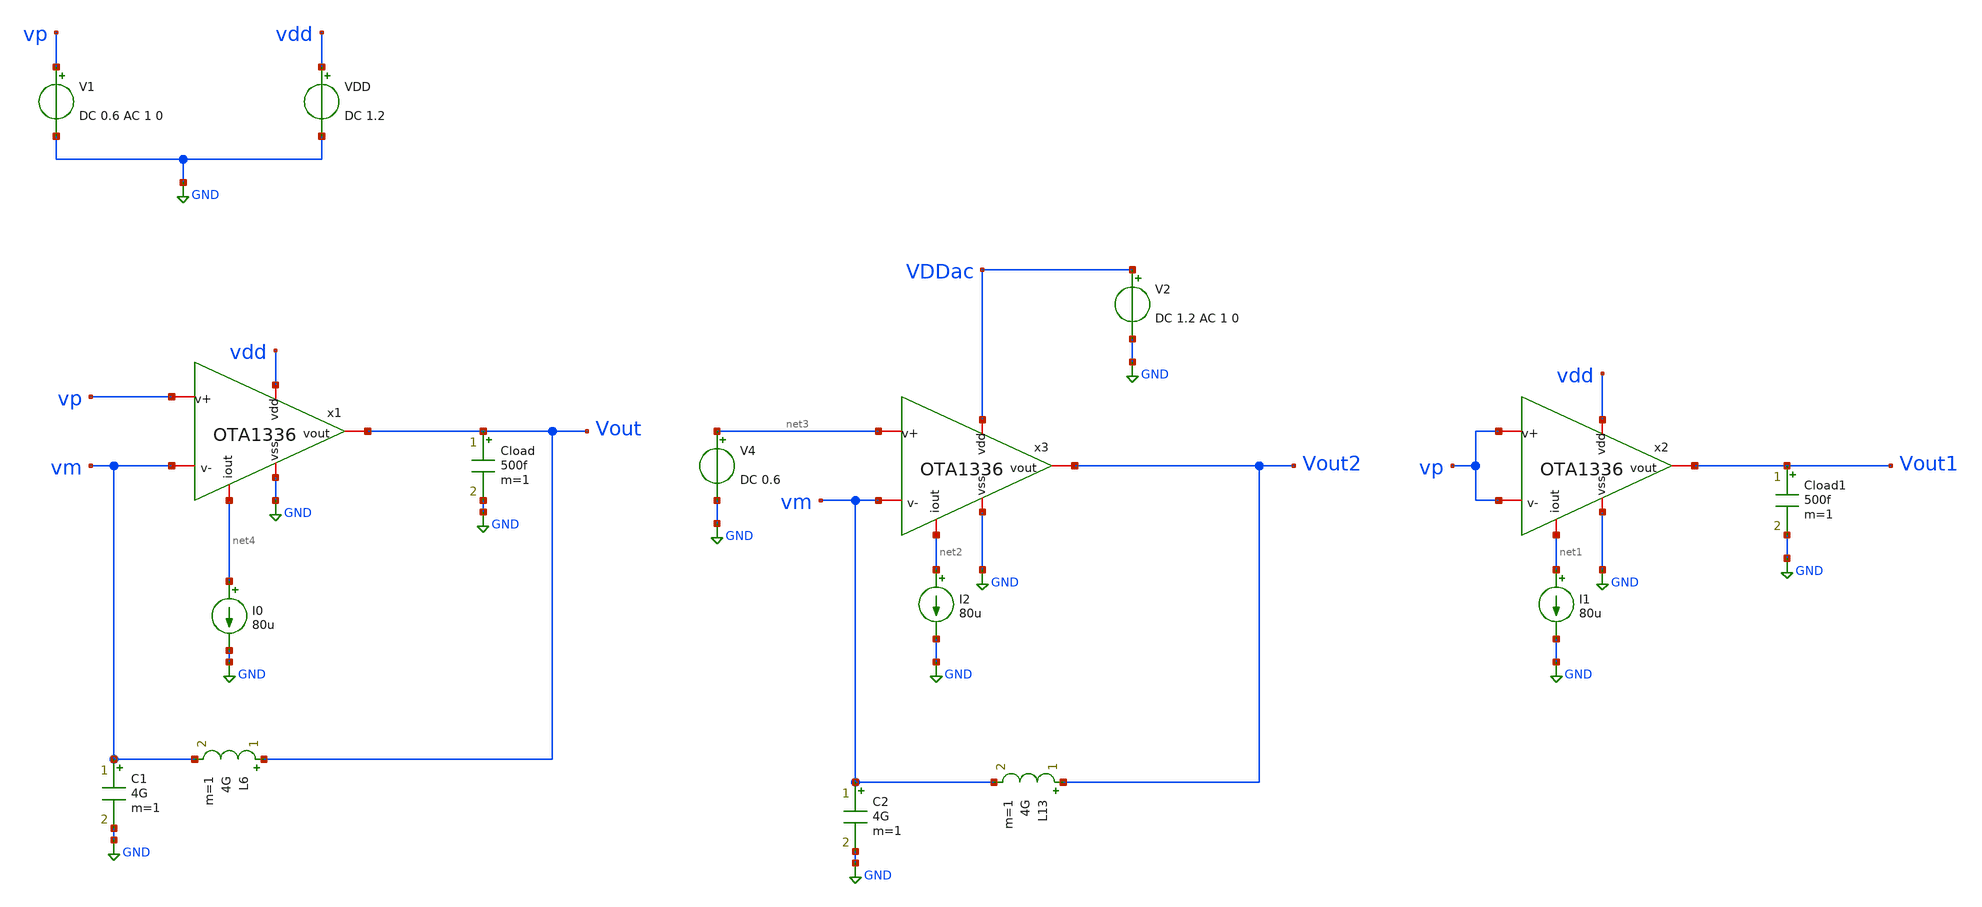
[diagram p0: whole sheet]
** sch_path: OTA1336-main/testbenches/ac/xschem/OTA1336_tb.sch
**.subckt OTA1336_tb
V1 vp GND DC 0.6 AC 1 0
VDD vdd GND DC 1.2
I0 net4 GND 80u
Cload Vout GND 500f m=1
L6 Vout vm 4G m=1
C1 vm GND 4G m=1
I1 net1 GND 80u
Cload1 Vout1 GND 500f m=1
I2 net2 GND 80u
L13 Vout2 vm 4G m=1
C2 vm GND 4G m=1
V2 VDDac GND DC 1.2 AC 1 0
V4 net3 GND DC 0.6
x1 vdd net4 Vout vm vp GND OTA1336
x2 vdd net1 Vout1 vp vp GND OTA1336
x3 VDDac net2 Vout2 vm net3 GND OTA1336
**** begin user architecture code

.lib cornerCAP.lib cap_typ
.lib cornerMOSlv.lib mos_tt
.lib cornerRES.lib res_typ



.control
op
save all
write tb_OTA_op.raw
.endc

.control
op
ac dec 100 1 10e7
save all
let Av = db(v(vout) / v(vp))
let vph = -180*unwrap(phase(V(vout)) - phase(V(vp)))/pi
let PSRR_linear = v(vout2)/v(VDDac)
let CMRR = db((v(vout)/v(vp))/(v(vout1)/v(vp)))
let phase = 180*cph(vout)/pi

let vog = db(V(vout)/V(vp))
let vph = 180 * unwrap(phase(V(vout)) - phase(V(vp)))/pi
let fbw = 0
let pm = 0
let gm = minimum(vog)
meas ac fbw WHEN vog=1 FALL=1
meas ac pm FIND vph WHEN vog=0 FALL=1
meas ac gm FIND vog WHEN vph=-180 FALL=1

let gainbw = $&fbw
let gmargin = $&gm
let pmargin = 180 + $&pm

print gainbw gmargin pmargin

write output_file.raw
.endc


**** end user architecture code
**.ends
.GLOBAL GND
.end
